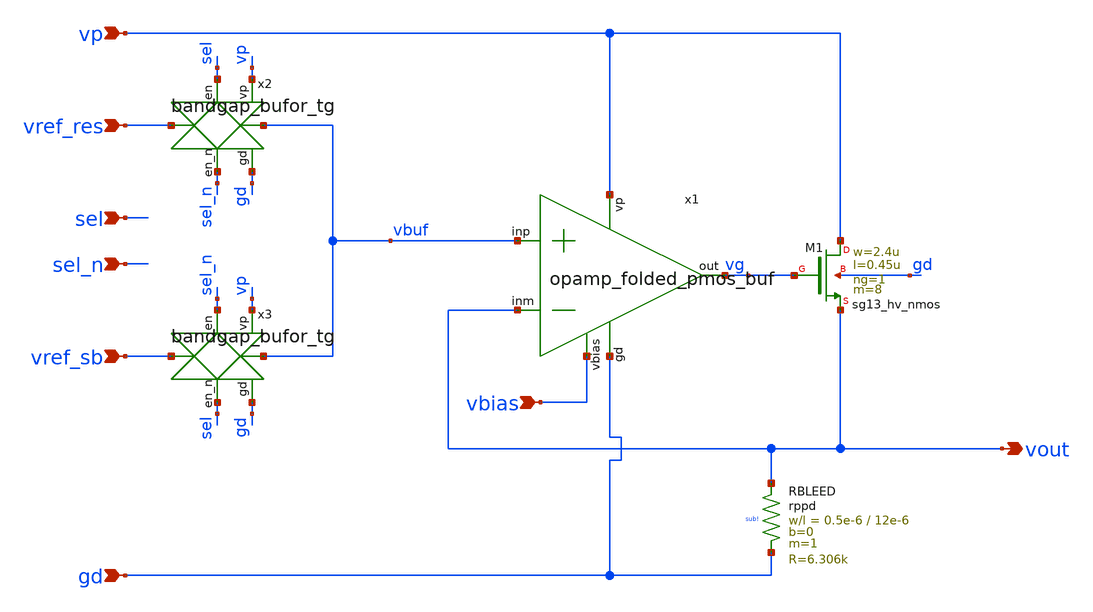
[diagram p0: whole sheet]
** sch_path: circuit/bandgap_buf_core.sch
**.subckt bandgap_buf_core vbias gd vp vref_res vref_sb vout sel sel_n
*.ipin vbias
*.ipin gd
*.ipin vp
*.ipin vref_res
*.ipin vref_sb
*.opin vout
*.ipin sel
*.ipin sel_n
x1 vp vbuf vout vg vbias gd opamp_folded_pmos_buf
x2 vbuf vref_res sel_n sel vp gd bandgap_bufor_tg
x3 vbuf vref_sb sel sel_n vp gd bandgap_bufor_tg
XM1 vp vg vout gd sg13_hv_nmos w=2.4u l=0.45u ng=1 m=8 mm_ok=1
XRBLEED vout gd sub! rppd w=0.5e-6 l=12e-6 m=1 b=0 mm_ok=1
**.ends

* expanding   symbol:  /foss/designs/test/circuit/opamp_folded_pmos_buf.sym # of pins=6
** sym_path: circuit/opamp_folded_pmos_buf.sym
** sch_path: circuit/opamp_folded_pmos_buf.sch
.subckt opamp_folded_pmos_buf vp inp inm out vbias gd
*.ipin vbias
*.ipin inp
*.ipin inm
*.opin out
*.ipin gd
*.ipin vp
XM12 bias4 vbias gd gd sg13_hv_nmos w=1.2u l=0.9u ng=1 m=2 mm_ok=1
XM13 bias4 bias4 vp vp sg13_hv_pmos w=3.6u l=0.9u ng=1 m=2 mm_ok=1
XM11 pair_com bias4 vp vp sg13_hv_pmos w=3.6u l=0.9u ng=1 m=4 mm_ok=1
XM1 inp_fold inp pair_com vp sg13_hv_pmos w=2.4u l=0.9u ng=1 m=12 mm_ok=1
XM2 inm_fold inm pair_com vp sg13_hv_pmos w=2.4u l=0.9u ng=1 m=12 mm_ok=1
XM9 tele_m tele_g vp vp sg13_hv_pmos w=3.6u l=0.9u ng=1 m=2 mm_ok=1
XM10 tele_p tele_g vp vp sg13_hv_pmos w=3.6u l=0.9u ng=1 m=2 mm_ok=1
XM7 tele_g bias3 tele_m vp sg13_hv_pmos w=3.6u l=0.9u ng=1 m=2 mm_ok=1
XM8 out bias3 tele_p vp sg13_hv_pmos w=3.6u l=0.9u ng=1 m=2 mm_ok=1
XM3 inp_fold vbias gd gd sg13_hv_nmos w=1.2u l=0.9u ng=1 m=4 mm_ok=1
XM4 inm_fold vbias gd gd sg13_hv_nmos w=1.2u l=0.9u ng=1 m=4 mm_ok=1
XM5 tele_g bias2 inp_fold gd sg13_hv_nmos w=1.2u l=0.9u ng=1 m=2 mm_ok=1
XM6 out bias2 inm_fold gd sg13_hv_nmos w=1.2u l=0.9u ng=1 m=2 mm_ok=1
XM14 bias3 vbias gd gd sg13_hv_nmos w=1.2u l=0.9u ng=1 m=4 mm_ok=1
XM15 bias3 bias3 net1 vp sg13_hv_pmos w=3.6u l=0.9u ng=1 m=1 mm_ok=1
XM16 net1 bias3 vp vp sg13_hv_pmos w=3.6u l=0.9u ng=1 m=1 mm_ok=1
XM19 bias2 bias4 vp vp sg13_hv_pmos w=3.6u l=0.9u ng=1 m=4 mm_ok=1
XM17 net2 bias2 gd gd sg13_hv_nmos w=1.2u l=0.9u ng=1 m=1 mm_ok=1
XM18 bias2 bias2 net2 gd sg13_hv_nmos w=1.2u l=0.9u ng=1 m=1 mm_ok=1
XM20 bias2 gd gd gd sg13_hv_nmos w=1.2u l=0.9u ng=1 m=1 mm_ok=1
XM21 pair_com vp vp vp sg13_hv_pmos w=2.4u l=0.9u ng=1 m=2 mm_ok=1
XM22 bias3 vp vp vp sg13_hv_pmos w=3.6u l=0.9u ng=1 m=1 mm_ok=1
.ends


* expanding   symbol:  /foss/designs/test/circuit/bandgap_bufor_tg.sym # of pins=6
** sym_path: circuit/bandgap_bufor_tg.sym
** sch_path: circuit/bandgap_bufor_tg.sch
.subckt bandgap_bufor_tg t2 t1 en_n en vp gd
*.ipin en_n
*.ipin en
*.ipin vp
*.ipin gd
*.iopin t2
*.iopin t1
XM1 t2 en t1 gd sg13_hv_nmos w=1.2u l=0.9u ng=1 m=2 mm_ok=1
XM2 t2 en_n t1 vp sg13_hv_pmos w=1.2u l=0.9u ng=1 m=2 mm_ok=1
.ends

.end
